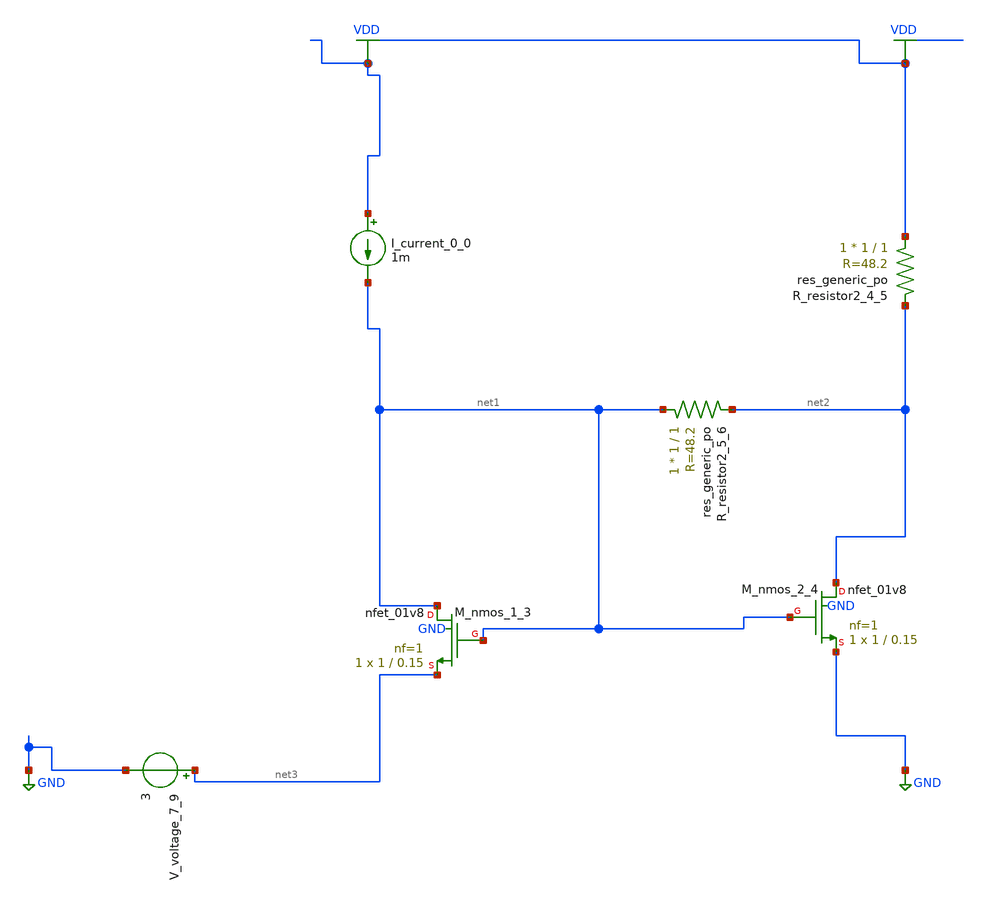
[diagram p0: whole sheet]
** sch_path: schematics/AMSNet/329.sch
**.subckt 329
I_current_0_0 VDD net1 1m
XM_nmos_1_3 net1 net1 net3 GND sky130_fd_pr__nfet_01v8 L=0.15 W=1 nf=1 ad='int((1 + 1)/2) * 1 / 1 * 0.29'
+ as='int((1 + 2)/2) * 1 / 1 * 0.29' pd='2*int((1 + 1)/2) * (1 / 1 + 0.29)' ps='2*int((1 + 2)/2) * (1 / 1 + 0.29)'
+ nrd='0.29 / 1 ' nrs='0.29 / 1 ' sa=0 sb=0 sd=0 mult=1 m=1
XM_nmos_2_4 net2 net1 GND GND sky130_fd_pr__nfet_01v8 L=0.15 W=1 nf=1 ad='int((1 + 1)/2) * 1 / 1 * 0.29'
+ as='int((1 + 2)/2) * 1 / 1 * 0.29' pd='2*int((1 + 1)/2) * (1 / 1 + 0.29)' ps='2*int((1 + 2)/2) * (1 / 1 + 0.29)'
+ nrd='0.29 / 1 ' nrs='0.29 / 1 ' sa=0 sb=0 sd=0 mult=1 m=1
XR_resistor2_4_5 VDD net2 sky130_fd_pr__res_generic_po W=1 L=1 m=1
XR_resistor2_5_6 net1 net2 sky130_fd_pr__res_generic_po W=1 L=1 m=1
V_voltage_7_9 net3 GND 3
**.ends
.GLOBAL GND
.GLOBAL VDD
.end
